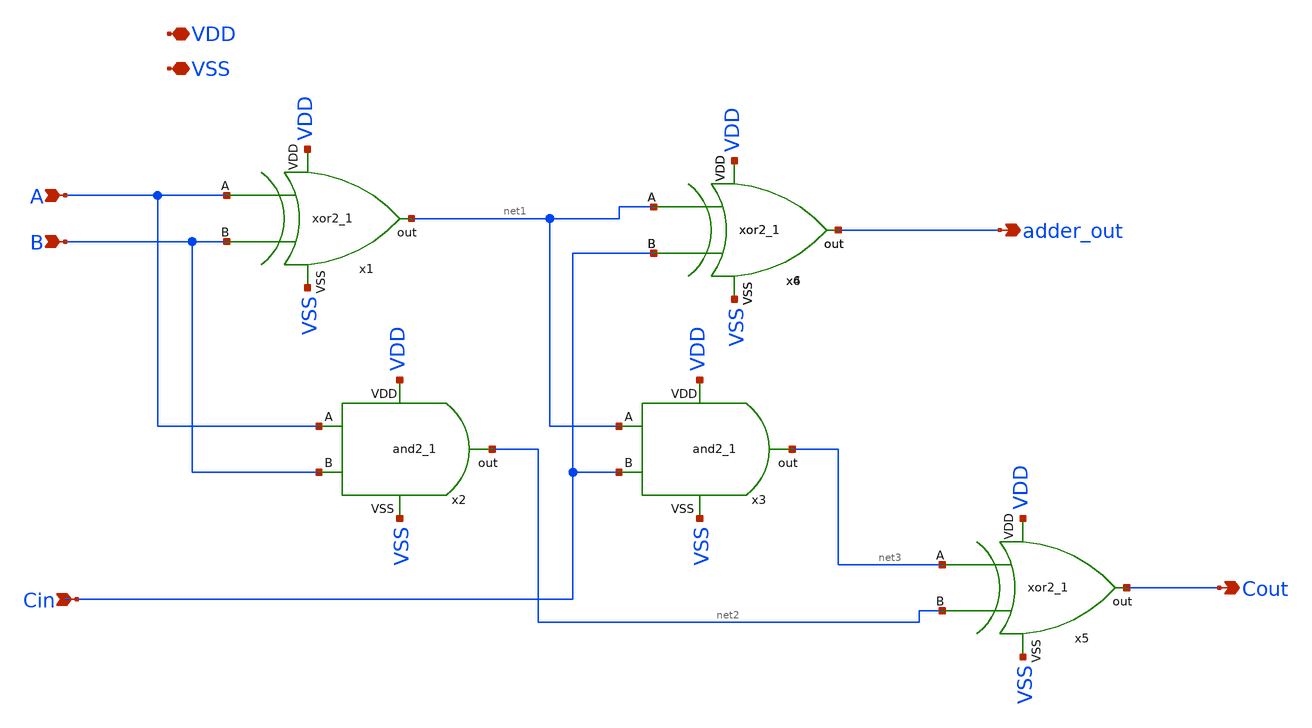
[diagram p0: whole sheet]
** sch_path: adder/1bit_adder.sch
**.subckt 1bit_adder A B VDD VSS Cin Cout adder_out
*.ipin A
*.ipin B
*.iopin VDD
*.iopin VSS
*.ipin Cin
*.opin Cout
*.opin adder_out
x1 A B VDD VSS net1 xor2
x2 VSS VDD A net2 B and2
x3 VSS VDD net1 net3 Cin and2
x4 net1 Cin VDD VSS adder_out xor2
x5 net3 net2 VDD VSS Cout xor2
x6 net1 Cin VDD VSS adder_out xor2
**.ends

* expanding   symbol:  xor2/xor2.sym # of pins=5
** sym_path: xor2/xor2.sym
** sch_path: xor2/xor2.sch
.subckt xor2 A B VDD VSS out
*.ipin A
*.ipin B
*.opin out
*.ipin VDD
*.ipin VSS
XM1 out notA net3 net3 sky130_fd_pr__nfet_01v8 L=0.15 W=1 nf=1 ad='int((nf+1)/2) * W/nf * 0.29' as='int((nf+2)/2) * W/nf * 0.29'
+ pd='2*int((nf+1)/2) * (W/nf + 0.29)' ps='2*int((nf+2)/2) * (W/nf + 0.29)' nrd='0.29 / W' nrs='0.29 / W'
+ sa=0 sb=0 sd=0 mult=1 m=1
XM2 out B net1 net1 sky130_fd_pr__pfet_01v8 L=0.15 W=1 nf=1 ad='int((nf+1)/2) * W/nf * 0.29' as='int((nf+2)/2) * W/nf * 0.29'
+ pd='2*int((nf+1)/2) * (W/nf + 0.29)' ps='2*int((nf+2)/2) * (W/nf + 0.29)' nrd='0.29 / W' nrs='0.29 / W'
+ sa=0 sb=0 sd=0 mult=1 m=1
XM3 net3 notB VSS VSS sky130_fd_pr__nfet_01v8 L=0.15 W=1 nf=1 ad='int((nf+1)/2) * W/nf * 0.29' as='int((nf+2)/2) * W/nf * 0.29'
+ pd='2*int((nf+1)/2) * (W/nf + 0.29)' ps='2*int((nf+2)/2) * (W/nf + 0.29)' nrd='0.29 / W' nrs='0.29 / W'
+ sa=0 sb=0 sd=0 mult=1 m=1
XM4 net1 notA VDD VDD sky130_fd_pr__pfet_01v8 L=0.15 W=1 nf=1 ad='int((nf+1)/2) * W/nf * 0.29' as='int((nf+2)/2) * W/nf * 0.29'
+ pd='2*int((nf+1)/2) * (W/nf + 0.29)' ps='2*int((nf+2)/2) * (W/nf + 0.29)' nrd='0.29 / W' nrs='0.29 / W'
+ sa=0 sb=0 sd=0 mult=1 m=1
XM5 net4 A VDD VDD sky130_fd_pr__pfet_01v8 L=0.15 W=1 nf=1 ad='int((nf+1)/2) * W/nf * 0.29' as='int((nf+2)/2) * W/nf * 0.29'
+ pd='2*int((nf+1)/2) * (W/nf + 0.29)' ps='2*int((nf+2)/2) * (W/nf + 0.29)' nrd='0.29 / W' nrs='0.29 / W'
+ sa=0 sb=0 sd=0 mult=1 m=1
XM6 out notB net4 net4 sky130_fd_pr__pfet_01v8 L=0.15 W=1 nf=1 ad='int((nf+1)/2) * W/nf * 0.29' as='int((nf+2)/2) * W/nf * 0.29'
+ pd='2*int((nf+1)/2) * (W/nf + 0.29)' ps='2*int((nf+2)/2) * (W/nf + 0.29)' nrd='0.29 / W' nrs='0.29 / W'
+ sa=0 sb=0 sd=0 mult=1 m=1
XM7 out A net2 net2 sky130_fd_pr__nfet_01v8 L=0.15 W=1 nf=1 ad='int((nf+1)/2) * W/nf * 0.29' as='int((nf+2)/2) * W/nf * 0.29'
+ pd='2*int((nf+1)/2) * (W/nf + 0.29)' ps='2*int((nf+2)/2) * (W/nf + 0.29)' nrd='0.29 / W' nrs='0.29 / W'
+ sa=0 sb=0 sd=0 mult=1 m=1
XM8 net2 B VSS VSS sky130_fd_pr__nfet_01v8 L=0.15 W=1 nf=1 ad='int((nf+1)/2) * W/nf * 0.29' as='int((nf+2)/2) * W/nf * 0.29'
+ pd='2*int((nf+1)/2) * (W/nf + 0.29)' ps='2*int((nf+2)/2) * (W/nf + 0.29)' nrd='0.29 / W' nrs='0.29 / W'
+ sa=0 sb=0 sd=0 mult=1 m=1
XM9 notA A VDD VDD sky130_fd_pr__pfet_01v8 L=0.15 W=1 nf=1 ad='int((nf+1)/2) * W/nf * 0.29' as='int((nf+2)/2) * W/nf * 0.29'
+ pd='2*int((nf+1)/2) * (W/nf + 0.29)' ps='2*int((nf+2)/2) * (W/nf + 0.29)' nrd='0.29 / W' nrs='0.29 / W'
+ sa=0 sb=0 sd=0 mult=1 m=1
XM10 notA A VSS VSS sky130_fd_pr__nfet_01v8 L=0.15 W=1 nf=1 ad='int((nf+1)/2) * W/nf * 0.29' as='int((nf+2)/2) * W/nf * 0.29'
+ pd='2*int((nf+1)/2) * (W/nf + 0.29)' ps='2*int((nf+2)/2) * (W/nf + 0.29)' nrd='0.29 / W' nrs='0.29 / W'
+ sa=0 sb=0 sd=0 mult=1 m=1
XM11 notB B VDD VDD sky130_fd_pr__pfet_01v8 L=0.15 W=1 nf=1 ad='int((nf+1)/2) * W/nf * 0.29' as='int((nf+2)/2) * W/nf * 0.29'
+ pd='2*int((nf+1)/2) * (W/nf + 0.29)' ps='2*int((nf+2)/2) * (W/nf + 0.29)' nrd='0.29 / W' nrs='0.29 / W'
+ sa=0 sb=0 sd=0 mult=1 m=1
XM12 notB B VSS VSS sky130_fd_pr__nfet_01v8 L=0.15 W=1 nf=1 ad='int((nf+1)/2) * W/nf * 0.29' as='int((nf+2)/2) * W/nf * 0.29'
+ pd='2*int((nf+1)/2) * (W/nf + 0.29)' ps='2*int((nf+2)/2) * (W/nf + 0.29)' nrd='0.29 / W' nrs='0.29 / W'
+ sa=0 sb=0 sd=0 mult=1 m=1
.ends


* expanding   symbol:  and/and2.sym # of pins=5
** sym_path: and/and2.sym
** sch_path: and/and2.sch
.subckt and2 VSS VDD A out B
*.ipin VDD
*.ipin A
*.ipin B
*.ipin VSS
*.opin out
XM1 net1 A net2 net2 sky130_fd_pr__nfet_01v8 L=0.15 W=1 nf=1 ad='int((nf+1)/2) * W/nf * 0.29' as='int((nf+2)/2) * W/nf * 0.29'
+ pd='2*int((nf+1)/2) * (W/nf + 0.29)' ps='2*int((nf+2)/2) * (W/nf + 0.29)' nrd='0.29 / W' nrs='0.29 / W'
+ sa=0 sb=0 sd=0 mult=1 m=1
XM2 net1 A VDD VDD sky130_fd_pr__pfet_01v8 L=0.15 W=1 nf=1 ad='int((nf+1)/2) * W/nf * 0.29' as='int((nf+2)/2) * W/nf * 0.29'
+ pd='2*int((nf+1)/2) * (W/nf + 0.29)' ps='2*int((nf+2)/2) * (W/nf + 0.29)' nrd='0.29 / W' nrs='0.29 / W'
+ sa=0 sb=0 sd=0 mult=1 m=1
XM3 net2 B VSS VSS sky130_fd_pr__nfet_01v8 L=0.15 W=1 nf=1 ad='int((nf+1)/2) * W/nf * 0.29' as='int((nf+2)/2) * W/nf * 0.29'
+ pd='2*int((nf+1)/2) * (W/nf + 0.29)' ps='2*int((nf+2)/2) * (W/nf + 0.29)' nrd='0.29 / W' nrs='0.29 / W'
+ sa=0 sb=0 sd=0 mult=1 m=1
XM4 net1 B VDD VDD sky130_fd_pr__pfet_01v8 L=0.15 W=1 nf=1 ad='int((nf+1)/2) * W/nf * 0.29' as='int((nf+2)/2) * W/nf * 0.29'
+ pd='2*int((nf+1)/2) * (W/nf + 0.29)' ps='2*int((nf+2)/2) * (W/nf + 0.29)' nrd='0.29 / W' nrs='0.29 / W'
+ sa=0 sb=0 sd=0 mult=1 m=1
XM5 out net1 VDD VDD sky130_fd_pr__pfet_01v8 L=0.15 W=1 nf=1 ad='int((nf+1)/2) * W/nf * 0.29' as='int((nf+2)/2) * W/nf * 0.29'
+ pd='2*int((nf+1)/2) * (W/nf + 0.29)' ps='2*int((nf+2)/2) * (W/nf + 0.29)' nrd='0.29 / W' nrs='0.29 / W'
+ sa=0 sb=0 sd=0 mult=1 m=1
XM6 out net1 VSS VSS sky130_fd_pr__nfet_01v8 L=0.15 W=1 nf=1 ad='int((nf+1)/2) * W/nf * 0.29' as='int((nf+2)/2) * W/nf * 0.29'
+ pd='2*int((nf+1)/2) * (W/nf + 0.29)' ps='2*int((nf+2)/2) * (W/nf + 0.29)' nrd='0.29 / W' nrs='0.29 / W'
+ sa=0 sb=0 sd=0 mult=1 m=1
.ends

.end
